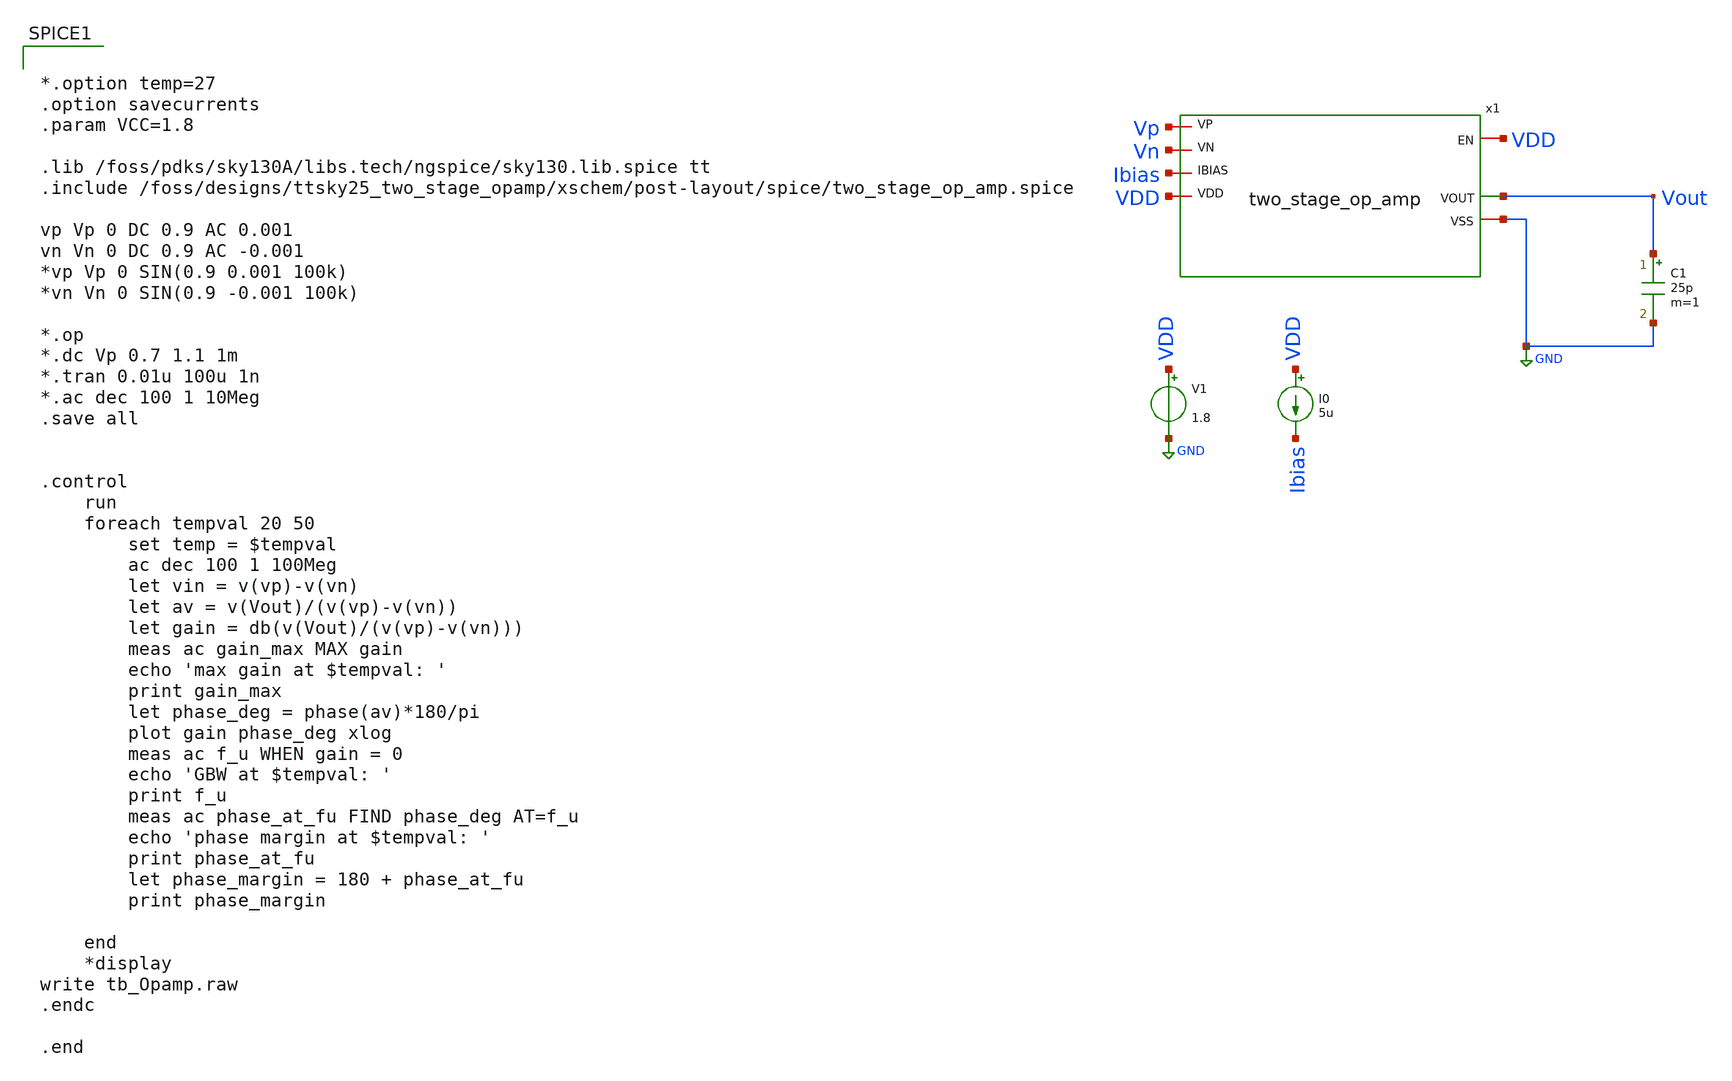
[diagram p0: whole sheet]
** sch_path: xschem/post-layout/testbenches/tb_Opamp.sch
**.subckt tb_Opamp
V1 VDD GND 1.8
C1 Vout GND 25p m=1
I0 VDD Ibias 5u
x1 Ibias VDD Vout Vn Vp VDD GND two_stage_op_amp
**** begin user architecture code


*.option temp=27
.option savecurrents
.param VCC=1.8

.lib /foss/pdks/sky130A/libs.tech/ngspice/sky130.lib.spice tt
.include /foss/designs/ttsky25_two_stage_opamp/xschem/post-layout/spice/two_stage_op_amp.spice

vp Vp 0 DC 0.9 AC 0.001
vn Vn 0 DC 0.9 AC -0.001
*vp Vp 0 SIN(0.9 0.001 100k)
*vn Vn 0 SIN(0.9 -0.001 100k)

*.op
*.dc Vp 0.7 1.1 1m
*.tran 0.01u 100u 1n
*.ac dec 100 1 10Meg
.save all


.control
	run
	foreach tempval 20 50
		set temp = $tempval
		ac dec 100 1 100Meg
		let vin = v(vp)-v(vn)
		let av = v(Vout)/(v(vp)-v(vn))
		let gain = db(v(Vout)/(v(vp)-v(vn)))
		meas ac gain_max MAX gain
		echo 'max gain at $tempval: '
		print gain_max
		let phase_deg = phase(av)*180/pi
		plot gain phase_deg xlog
		meas ac f_u WHEN gain = 0
		echo 'GBW at $tempval: '
		print f_u
		meas ac phase_at_fu FIND phase_deg AT=f_u
		echo 'phase margin at $tempval: '
		print phase_at_fu
		let phase_margin = 180 + phase_at_fu
		print phase_margin

	end
	*display
write tb_Opamp.raw
.endc

.end


**** end user architecture code
**.ends
.GLOBAL GND
.end
